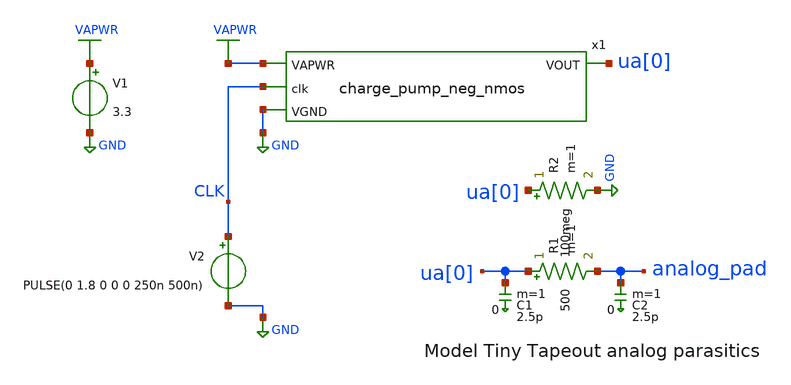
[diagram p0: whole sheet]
** sch_path: xschem/charge_pump_neg_tb.sch
**.subckt charge_pump_neg_tb
V1 VAPWR GND 3.3
V2 CLK GND PULSE(0 1.8 0 0 0 250n 500n)
R1 ua[0] analog_pad 500 m=1
C1 ua[0] 0 2.5p m=1
C2 analog_pad 0 2.5p m=1
R2 ua[0] GND 100meg m=1
x1 CLK ua[0] VAPWR GND charge_pump_neg_nmos
**** begin user architecture code

** opencircuitdesign pdks install
.lib $::SKYWATER_MODELS/sky130.lib.spice tt
.include ../../spice/charge_pump_neg_nmos/pex/charge_pump_neg_nmos.spice
*.include ../../spice/charge_pump_neg_nmos/sch/charge_pump_neg_nmos.spice




.tran 10n 100u
.save all
.options savecurrents

.control
run
write charge_pump_neg_tb.raw
.endc


**** end user architecture code
**.ends
.GLOBAL GND
.GLOBAL VAPWR
.end
